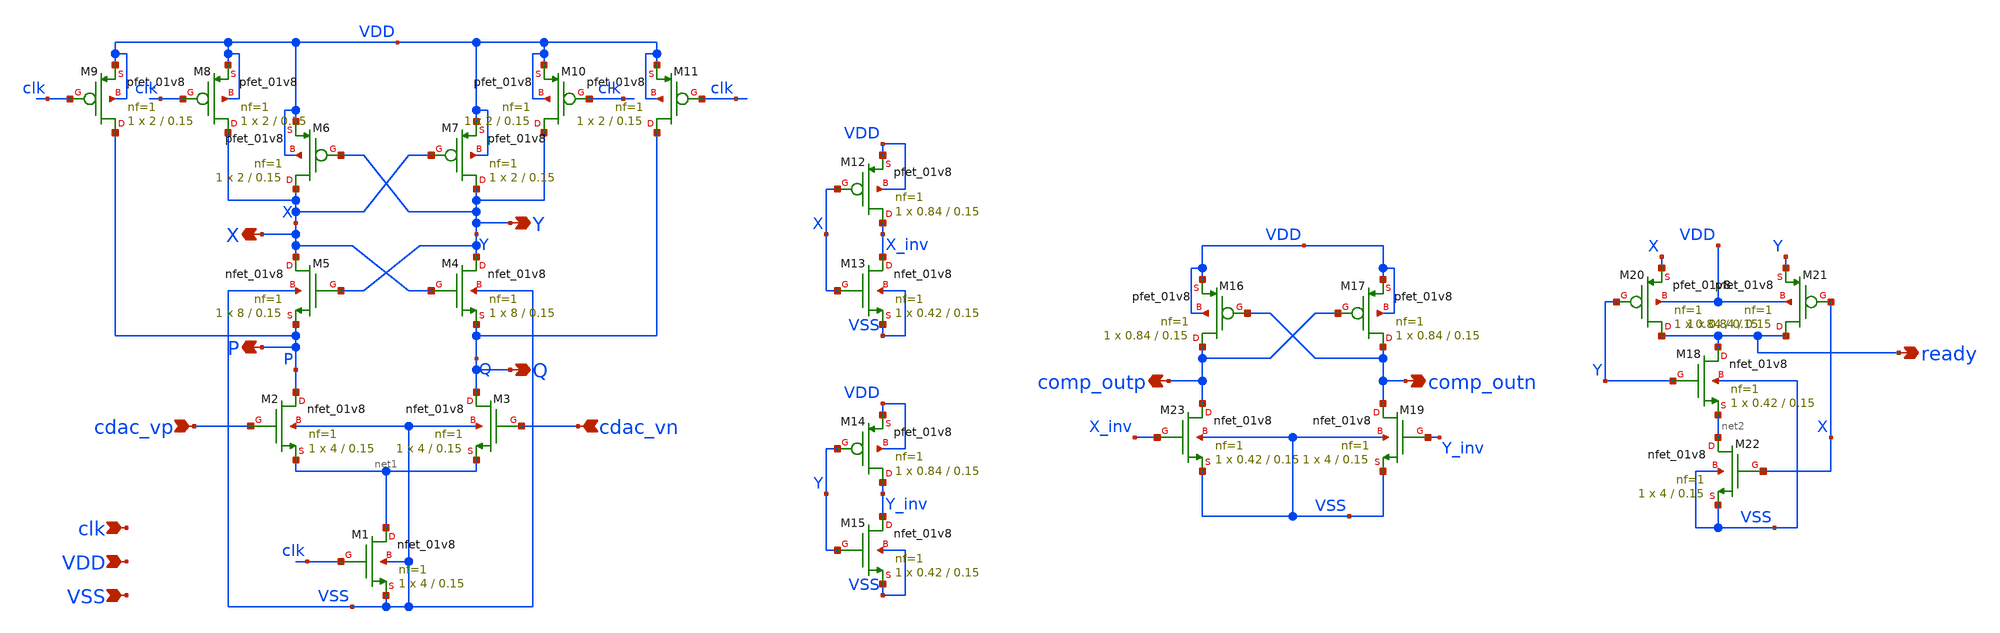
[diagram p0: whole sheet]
** sch_path: module/comparator/comp.sch
**.subckt comp cdac_vn cdac_vp VSS VDD comp_outp comp_outn ready clk X Y P Q
*.ipin cdac_vn
*.ipin cdac_vp
*.ipin VSS
*.ipin VDD
*.opin comp_outp
*.opin comp_outn
*.opin ready
*.ipin clk
*.opin X
*.opin Y
*.opin P
*.opin Q
XM1 net1 clk VSS VSS sky130_fd_pr__nfet_01v8 L=0.15 W=4 nf=1 ad='int((nf+1)/2) * W/nf * 0.29' as='int((nf+2)/2) * W/nf * 0.29'
+ pd='2*int((nf+1)/2) * (W/nf + 0.29)' ps='2*int((nf+2)/2) * (W/nf + 0.29)' nrd='0.29 / W' nrs='0.29 / W'
+ sa=0 sb=0 sd=0 mult=1 m=1
XM2 P cdac_vp net1 VSS sky130_fd_pr__nfet_01v8 L=0.15 W=4 nf=1 ad='int((nf+1)/2) * W/nf * 0.29' as='int((nf+2)/2) * W/nf * 0.29'
+ pd='2*int((nf+1)/2) * (W/nf + 0.29)' ps='2*int((nf+2)/2) * (W/nf + 0.29)' nrd='0.29 / W' nrs='0.29 / W'
+ sa=0 sb=0 sd=0 mult=1 m=1
XM3 Q cdac_vn net1 VSS sky130_fd_pr__nfet_01v8 L=0.15 W=4 nf=1 ad='int((nf+1)/2) * W/nf * 0.29' as='int((nf+2)/2) * W/nf * 0.29'
+ pd='2*int((nf+1)/2) * (W/nf + 0.29)' ps='2*int((nf+2)/2) * (W/nf + 0.29)' nrd='0.29 / W' nrs='0.29 / W'
+ sa=0 sb=0 sd=0 mult=1 m=1
XM4 Y X Q VSS sky130_fd_pr__nfet_01v8 L=0.15 W=8 nf=1 ad='int((nf+1)/2) * W/nf * 0.29' as='int((nf+2)/2) * W/nf * 0.29'
+ pd='2*int((nf+1)/2) * (W/nf + 0.29)' ps='2*int((nf+2)/2) * (W/nf + 0.29)' nrd='0.29 / W' nrs='0.29 / W'
+ sa=0 sb=0 sd=0 mult=1 m=1
XM5 X Y P VSS sky130_fd_pr__nfet_01v8 L=0.15 W=8 nf=1 ad='int((nf+1)/2) * W/nf * 0.29' as='int((nf+2)/2) * W/nf * 0.29'
+ pd='2*int((nf+1)/2) * (W/nf + 0.29)' ps='2*int((nf+2)/2) * (W/nf + 0.29)' nrd='0.29 / W' nrs='0.29 / W'
+ sa=0 sb=0 sd=0 mult=1 m=1
XM6 X Y VDD VDD sky130_fd_pr__pfet_01v8 L=0.15 W=2 nf=1 ad='int((nf+1)/2) * W/nf * 0.29' as='int((nf+2)/2) * W/nf * 0.29'
+ pd='2*int((nf+1)/2) * (W/nf + 0.29)' ps='2*int((nf+2)/2) * (W/nf + 0.29)' nrd='0.29 / W' nrs='0.29 / W'
+ sa=0 sb=0 sd=0 mult=1 m=1
XM7 Y X VDD VDD sky130_fd_pr__pfet_01v8 L=0.15 W=2 nf=1 ad='int((nf+1)/2) * W/nf * 0.29' as='int((nf+2)/2) * W/nf * 0.29'
+ pd='2*int((nf+1)/2) * (W/nf + 0.29)' ps='2*int((nf+2)/2) * (W/nf + 0.29)' nrd='0.29 / W' nrs='0.29 / W'
+ sa=0 sb=0 sd=0 mult=1 m=1
XM8 X clk VDD VDD sky130_fd_pr__pfet_01v8 L=0.15 W=2 nf=1 ad='int((nf+1)/2) * W/nf * 0.29' as='int((nf+2)/2) * W/nf * 0.29'
+ pd='2*int((nf+1)/2) * (W/nf + 0.29)' ps='2*int((nf+2)/2) * (W/nf + 0.29)' nrd='0.29 / W' nrs='0.29 / W'
+ sa=0 sb=0 sd=0 mult=1 m=1
XM9 P clk VDD VDD sky130_fd_pr__pfet_01v8 L=0.15 W=2 nf=1 ad='int((nf+1)/2) * W/nf * 0.29' as='int((nf+2)/2) * W/nf * 0.29'
+ pd='2*int((nf+1)/2) * (W/nf + 0.29)' ps='2*int((nf+2)/2) * (W/nf + 0.29)' nrd='0.29 / W' nrs='0.29 / W'
+ sa=0 sb=0 sd=0 mult=1 m=1
XM10 Y clk VDD VDD sky130_fd_pr__pfet_01v8 L=0.15 W=2 nf=1 ad='int((nf+1)/2) * W/nf * 0.29' as='int((nf+2)/2) * W/nf * 0.29'
+ pd='2*int((nf+1)/2) * (W/nf + 0.29)' ps='2*int((nf+2)/2) * (W/nf + 0.29)' nrd='0.29 / W' nrs='0.29 / W'
+ sa=0 sb=0 sd=0 mult=1 m=1
XM11 Q clk VDD VDD sky130_fd_pr__pfet_01v8 L=0.15 W=2 nf=1 ad='int((nf+1)/2) * W/nf * 0.29' as='int((nf+2)/2) * W/nf * 0.29'
+ pd='2*int((nf+1)/2) * (W/nf + 0.29)' ps='2*int((nf+2)/2) * (W/nf + 0.29)' nrd='0.29 / W' nrs='0.29 / W'
+ sa=0 sb=0 sd=0 mult=1 m=1
XM12 X_inv X VDD VDD sky130_fd_pr__pfet_01v8 L=0.15 W=0.84 nf=1 ad='int((nf+1)/2) * W/nf * 0.29' as='int((nf+2)/2) * W/nf * 0.29'
+ pd='2*int((nf+1)/2) * (W/nf + 0.29)' ps='2*int((nf+2)/2) * (W/nf + 0.29)' nrd='0.29 / W' nrs='0.29 / W'
+ sa=0 sb=0 sd=0 mult=1 m=1
XM13 X_inv X VSS VSS sky130_fd_pr__nfet_01v8 L=0.15 W=0.42 nf=1 ad='int((nf+1)/2) * W/nf * 0.29' as='int((nf+2)/2) * W/nf * 0.29'
+ pd='2*int((nf+1)/2) * (W/nf + 0.29)' ps='2*int((nf+2)/2) * (W/nf + 0.29)' nrd='0.29 / W' nrs='0.29 / W'
+ sa=0 sb=0 sd=0 mult=1 m=1
XM14 Y_inv Y VDD VDD sky130_fd_pr__pfet_01v8 L=0.15 W=0.84 nf=1 ad='int((nf+1)/2) * W/nf * 0.29' as='int((nf+2)/2) * W/nf * 0.29'
+ pd='2*int((nf+1)/2) * (W/nf + 0.29)' ps='2*int((nf+2)/2) * (W/nf + 0.29)' nrd='0.29 / W' nrs='0.29 / W'
+ sa=0 sb=0 sd=0 mult=1 m=1
XM15 Y_inv Y VSS VSS sky130_fd_pr__nfet_01v8 L=0.15 W=0.42 nf=1 ad='int((nf+1)/2) * W/nf * 0.29' as='int((nf+2)/2) * W/nf * 0.29'
+ pd='2*int((nf+1)/2) * (W/nf + 0.29)' ps='2*int((nf+2)/2) * (W/nf + 0.29)' nrd='0.29 / W' nrs='0.29 / W'
+ sa=0 sb=0 sd=0 mult=1 m=1
XM16 comp_outp comp_outn VDD VDD sky130_fd_pr__pfet_01v8 L=0.15 W=0.84 nf=1 ad='int((nf+1)/2) * W/nf * 0.29'
+ as='int((nf+2)/2) * W/nf * 0.29' pd='2*int((nf+1)/2) * (W/nf + 0.29)' ps='2*int((nf+2)/2) * (W/nf + 0.29)'
+ nrd='0.29 / W' nrs='0.29 / W' sa=0 sb=0 sd=0 mult=1 m=1
XM17 comp_outn comp_outp VDD VDD sky130_fd_pr__pfet_01v8 L=0.15 W=0.84 nf=1 ad='int((nf+1)/2) * W/nf * 0.29'
+ as='int((nf+2)/2) * W/nf * 0.29' pd='2*int((nf+1)/2) * (W/nf + 0.29)' ps='2*int((nf+2)/2) * (W/nf + 0.29)'
+ nrd='0.29 / W' nrs='0.29 / W' sa=0 sb=0 sd=0 mult=1 m=1
XM18 ready Y net2 VSS sky130_fd_pr__nfet_01v8 L=0.15 W=0.42 nf=1 ad='int((nf+1)/2) * W/nf * 0.29' as='int((nf+2)/2) * W/nf * 0.29'
+ pd='2*int((nf+1)/2) * (W/nf + 0.29)' ps='2*int((nf+2)/2) * (W/nf + 0.29)' nrd='0.29 / W' nrs='0.29 / W'
+ sa=0 sb=0 sd=0 mult=1 m=1
XM19 comp_outn Y_inv VSS VSS sky130_fd_pr__nfet_01v8 L=0.15 W=4 nf=1 ad='int((nf+1)/2) * W/nf * 0.29'
+ as='int((nf+2)/2) * W/nf * 0.29' pd='2*int((nf+1)/2) * (W/nf + 0.29)' ps='2*int((nf+2)/2) * (W/nf + 0.29)'
+ nrd='0.29 / W' nrs='0.29 / W' sa=0 sb=0 sd=0 mult=1 m=1
XM20 ready Y X VDD sky130_fd_pr__pfet_01v8 L=0.15 W=0.84 nf=1 ad='int((nf+1)/2) * W/nf * 0.29' as='int((nf+2)/2) * W/nf * 0.29'
+ pd='2*int((nf+1)/2) * (W/nf + 0.29)' ps='2*int((nf+2)/2) * (W/nf + 0.29)' nrd='0.29 / W' nrs='0.29 / W'
+ sa=0 sb=0 sd=0 mult=1 m=1
XM21 ready X Y VDD sky130_fd_pr__pfet_01v8 L=0.15 W=0.84 nf=1 ad='int((nf+1)/2) * W/nf * 0.29' as='int((nf+2)/2) * W/nf * 0.29'
+ pd='2*int((nf+1)/2) * (W/nf + 0.29)' ps='2*int((nf+2)/2) * (W/nf + 0.29)' nrd='0.29 / W' nrs='0.29 / W'
+ sa=0 sb=0 sd=0 mult=1 m=1
XM22 net2 X VSS VSS sky130_fd_pr__nfet_01v8 L=0.15 W=4 nf=1 ad='int((nf+1)/2) * W/nf * 0.29' as='int((nf+2)/2) * W/nf * 0.29'
+ pd='2*int((nf+1)/2) * (W/nf + 0.29)' ps='2*int((nf+2)/2) * (W/nf + 0.29)' nrd='0.29 / W' nrs='0.29 / W'
+ sa=0 sb=0 sd=0 mult=1 m=1
XM23 comp_outp X_inv VSS VSS sky130_fd_pr__nfet_01v8 L=0.15 W=0.42 nf=1 ad='int((nf+1)/2) * W/nf * 0.29'
+ as='int((nf+2)/2) * W/nf * 0.29' pd='2*int((nf+1)/2) * (W/nf + 0.29)' ps='2*int((nf+2)/2) * (W/nf + 0.29)'
+ nrd='0.29 / W' nrs='0.29 / W' sa=0 sb=0 sd=0 mult=1 m=1
**.ends
.end
